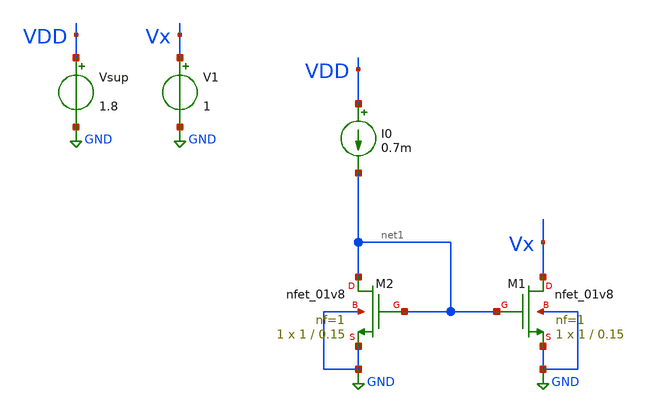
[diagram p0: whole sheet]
** sch_path: current_source_tb/currentsrc.sch
**.subckt currentsrc
XM1 Vx net1 GND GND sky130_fd_pr__nfet_01v8 L=0.15 W=1 nf=1 ad='int((nf+1)/2) * W/nf * 0.29' as='int((nf+2)/2) * W/nf * 0.29'
+ pd='2*int((nf+1)/2) * (W/nf + 0.29)' ps='2*int((nf+2)/2) * (W/nf + 0.29)' nrd='0.29 / W' nrs='0.29 / W'
+ sa=0 sb=0 sd=0 mult=1 m=1
XM2 net1 net1 GND GND sky130_fd_pr__nfet_01v8 L=0.15 W=1 nf=1 ad='int((nf+1)/2) * W/nf * 0.29' as='int((nf+2)/2) * W/nf * 0.29'
+ pd='2*int((nf+1)/2) * (W/nf + 0.29)' ps='2*int((nf+2)/2) * (W/nf + 0.29)' nrd='0.29 / W' nrs='0.29 / W'
+ sa=0 sb=0 sd=0 mult=1 m=1
V1 Vx GND 1
Vsup VDD GND 1.8
I0 VDD net1 0.7m
**** begin user architecture code


.option wnflag = 1
.lib /usr/local/share/pdk/sky130A/libs.tech/ngspice/sky130.lib.spice tt
.include /usr/local/share/pdk/sky130A/libs.ref/sky130_fd_pr/spice/sky130_fd_pr__ind_05_220.model.spice
.param mc_mm_switch=0


**** end user architecture code
**.ends
.GLOBAL GND
.end
